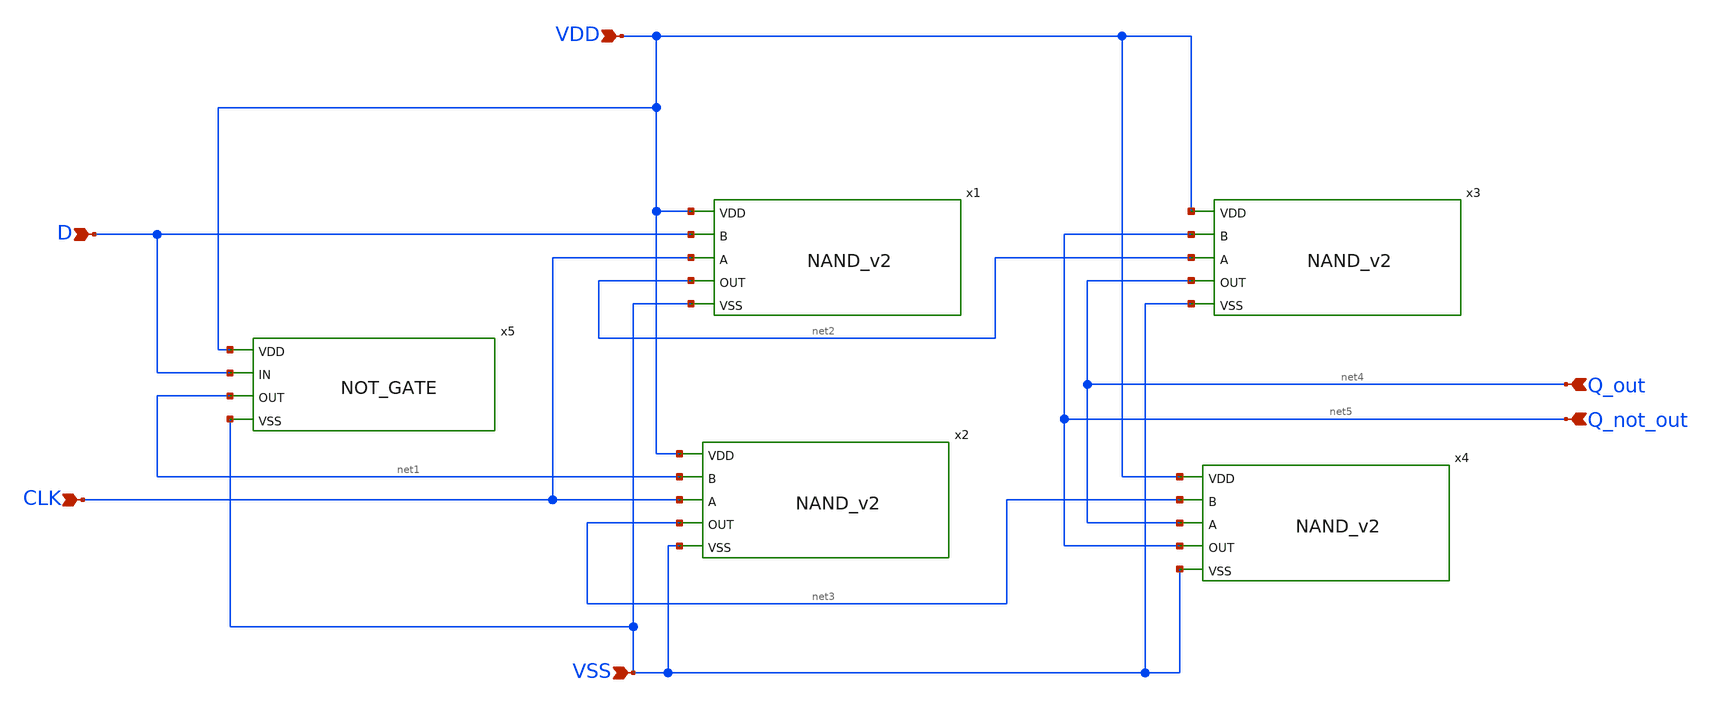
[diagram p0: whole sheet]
** sch_path: D_FLIP_FLOP.sch
**.subckt D_FLIP_FLOP VDD VSS D CLK Q_out Q_not_out
*.ipin VDD
*.ipin VSS
*.ipin D
*.ipin CLK
*.ipin Q_out
*.ipin Q_not_out
x5 VDD D net1 VSS NOT_GATE
x1 VDD D CLK net2 VSS NAND_v2
x2 VDD net1 CLK net3 VSS NAND_v2
x3 VDD net5 net2 net4 VSS NAND_v2
x4 VDD net3 net4 net5 VSS NAND_v2
**.ends
.end
